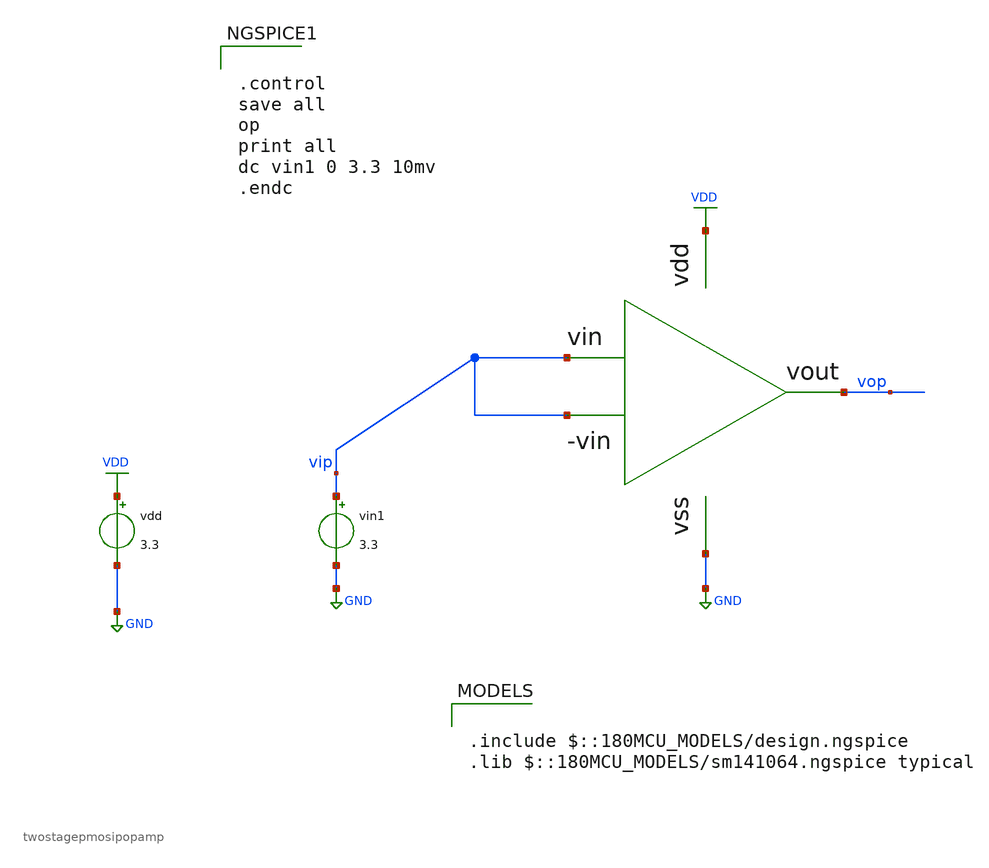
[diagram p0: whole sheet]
** sch_path: designs/First cut design/2stagepmosota.sch
**.subckt 2stagepmosota
vin1 vip GND 3.3
vdd VDD GND 3.3
xOTA1 vip VDD vip vop GND twostagepmosipopamp
**** begin user architecture code

.include $::180MCU_MODELS/design.ngspice
.lib $::180MCU_MODELS/sm141064.ngspice typical



.control
save all
op
print all
dc vin1 0 3.3 10mv
.endc

**** end user architecture code
**.ends
.GLOBAL GND
.GLOBAL VDD
.end
